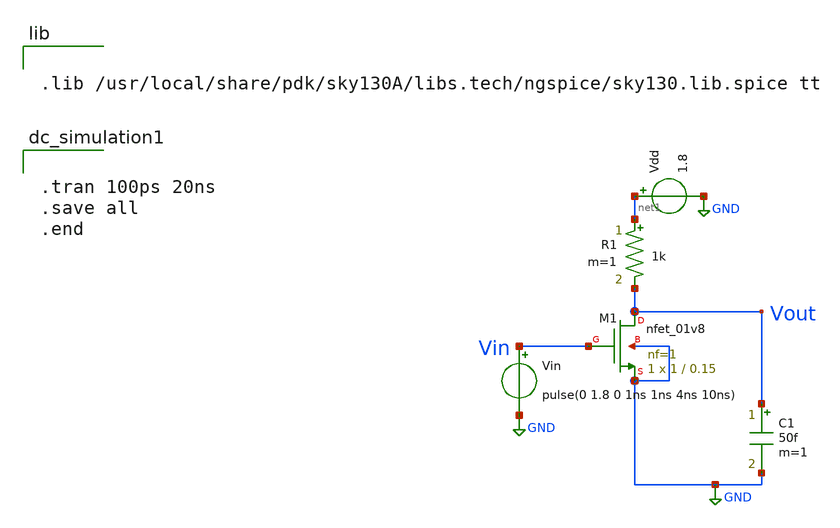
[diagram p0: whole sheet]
** sch_path: xschem/nmos.sch
**.subckt nmos
XM1 Vout Vin GND GND sky130_fd_pr__nfet_01v8 L=0.15 W=1 nf=1 ad='int((nf+1)/2) * W/nf * 0.29' as='int((nf+2)/2) * W/nf * 0.29'
+ pd='2*int((nf+1)/2) * (W/nf + 0.29)' ps='2*int((nf+2)/2) * (W/nf + 0.29)' nrd='0.29 / W' nrs='0.29 / W'
+ sa=0 sb=0 sd=0 mult=1 m=1
Vin Vin GND pulse(0 1.8 0 1ns 1ns 4ns 10ns)
Vdd net1 GND 1.8
R1 net1 Vout 1k m=1
C1 Vout GND 50f m=1
**** begin user architecture code


.lib /usr/local/share/pdk/sky130A/libs.tech/ngspice/sky130.lib.spice tt




.tran 100ps 20ns
.save all
.end


**** end user architecture code
**.ends
.GLOBAL GND
.end
